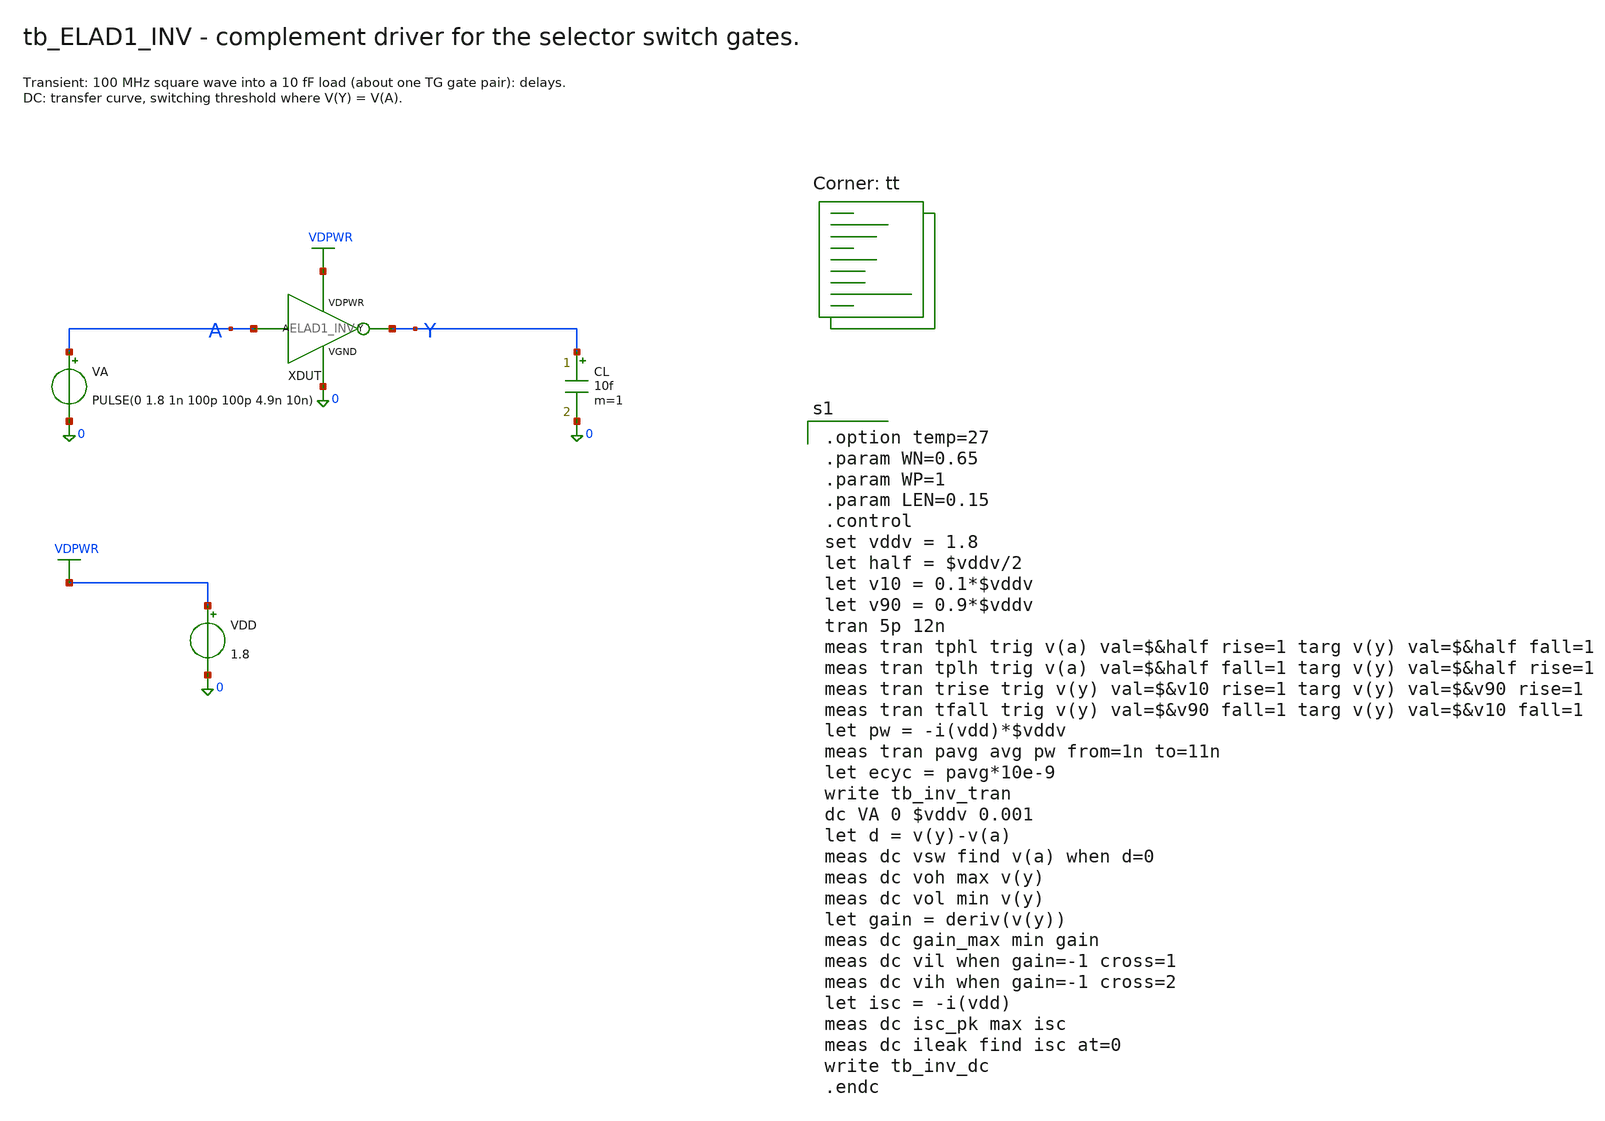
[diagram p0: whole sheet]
** sch_path: cells/ELAD1_INV/schematic/tb_ELAD1_INV.sch
**.subckt tb_ELAD1_INV
XDUT A Y VDPWR 0 ELAD1_INV
VA A 0 PULSE(0 1.8 1n 100p 100p 4.9n 10n)
CL Y 0 10f m=1
VDD VDPWR 0 1.8
**** begin user architecture code

.option temp=27
.param WN=0.65
.param WP=1
.param LEN=0.15
.control
set vddv = 1.8
let half = $vddv/2
let v10 = 0.1*$vddv
let v90 = 0.9*$vddv
tran 5p 12n
meas tran tphl trig v(a) val=$&half rise=1 targ v(y) val=$&half fall=1
meas tran tplh trig v(a) val=$&half fall=1 targ v(y) val=$&half rise=1
meas tran trise trig v(y) val=$&v10 rise=1 targ v(y) val=$&v90 rise=1
meas tran tfall trig v(y) val=$&v90 fall=1 targ v(y) val=$&v10 fall=1
let pw = -i(vdd)*$vddv
meas tran pavg avg pw from=1n to=11n
let ecyc = pavg*10e-9
write tb_inv_tran
dc VA 0 $vddv 0.001
let d = v(y)-v(a)
meas dc vsw find v(a) when d=0
meas dc voh max v(y)
meas dc vol min v(y)
let gain = deriv(v(y))
meas dc gain_max min gain
meas dc vil when gain=-1 cross=1
meas dc vih when gain=-1 cross=2
let isc = -i(vdd)
meas dc isc_pk max isc
meas dc ileak find isc at=0
write tb_inv_dc
.endc

.lib $::SKYWATER_MODELS/sky130.lib.spice tt
**** end user architecture code
**.ends

* expanding   symbol:  ELAD1_INV.sym # of pins=4
** sym_path: cells/ELAD1_INV/schematic/ELAD1_INV.sym
** sch_path: cells/ELAD1_INV/schematic/ELAD1_INV.sch
.subckt ELAD1_INV A Y VDPWR VGND
*.iopin A
*.iopin Y
*.iopin VDPWR
*.iopin VGND
XMN Y A VGND VGND sky130_fd_pr__nfet_01v8 L=0.15 W=0.65 nf=1 ad='int((1 + 1)/2) * 0.65 / 1 * 0.29' as='int((1 + 2)/2) * 0.65 / 1 * 0.29'
+ pd='2*int((1 + 1)/2) * (0.65 / 1 + 0.29)' ps='2*int((1 + 2)/2) * (0.65 / 1 + 0.29)' nrd='0.29 / 0.65 '
+ nrs='0.29 / 0.65 ' sa=0 sb=0 sd=0 mult=1 m=1
XMP Y A VDPWR VDPWR sky130_fd_pr__pfet_01v8 L=0.15 W=1 nf=1 ad='int((nf+1)/2) * W/nf * 0.29' as='int((nf+2)/2) * W/nf * 0.29'
+ pd='2*int((nf+1)/2) * (W/nf + 0.29)' ps='2*int((nf+2)/2) * (W/nf + 0.29)' nrd='0.29 / W' nrs='0.29 / W'
+ sa=0 sb=0 sd=0 mult=1 m=1
.ends

.GLOBAL VGND
.GLOBAL VDPWR
.end
